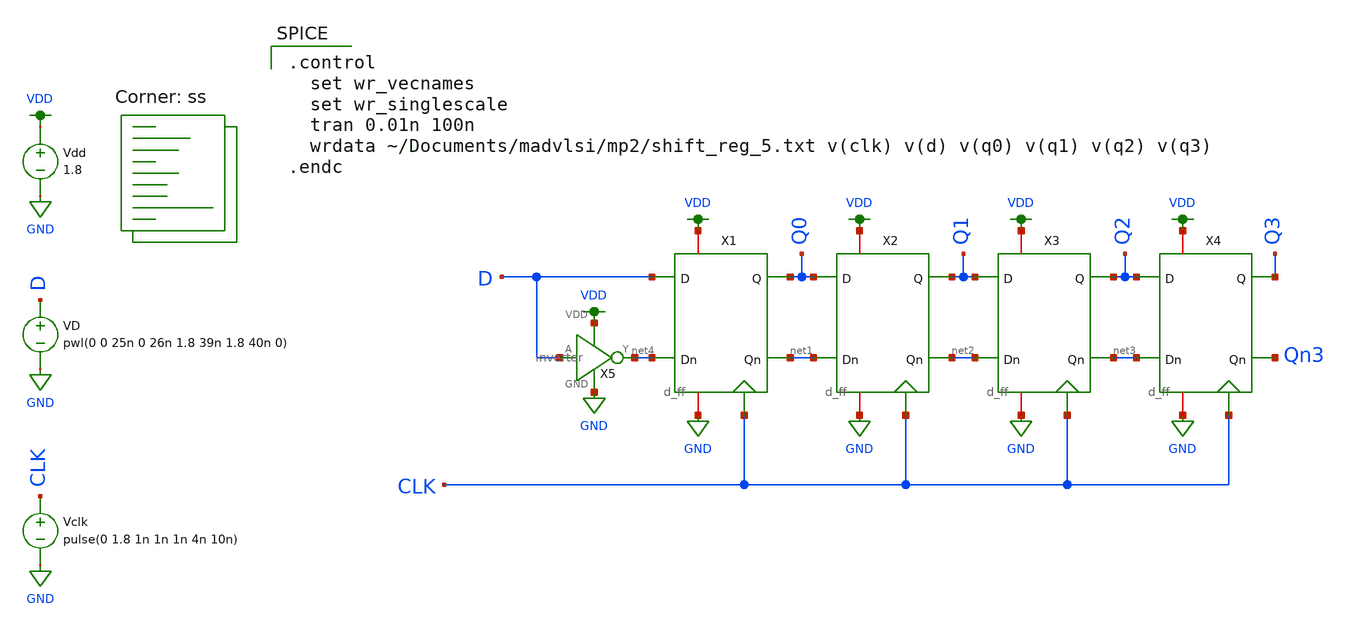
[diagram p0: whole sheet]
** sch_path: mp2/shift_reg_tb.sch
**.subckt shift_reg_tb
X5 VDD D net4 GND inverter
Vdd VDD GND 1.8
VD D GND pwl(0 0 25n 0 26n 1.8 39n 1.8 40n 0)
Vclk CLK GND pulse(0 1.8 1n 1n 1n 4n 10n)
X1 VDD Q0 D net4 net1 GND CLK d_ff
X2 VDD Q1 Q0 net1 net2 GND CLK d_ff
X3 VDD Q2 Q1 net2 net3 GND CLK d_ff
X4 VDD Q3 Q2 net3 Qn3 GND CLK d_ff
**** begin user architecture code
.lib $::SKYWATER_MODELS/sky130.lib.spice ss

.control
  set wr_vecnames
  set wr_singlescale
  tran 0.01n 100n
  wrdata ~/Documents/madvlsi/mp2/shift_reg_5.txt v(clk) v(d) v(q0) v(q1) v(q2) v(q3)
.endc

**** end user architecture code
**.ends

* expanding   symbol:  /home/dt/Documents/madvlsi/mp1/inverter.sym # of pins=4
** sym_path: final/schematics/inverter.sym
** sch_path: final/schematics/inverter.sch
.subckt inverter VDD A Y GND
*.ipin A
*.iopin VDD
*.iopin GND
*.opin Y
XM1 Y A GND GND sky130_fd_pr__nfet_01v8 L={len} W={wid} nf=1 ad='int((nf+1)/2) * W/nf * 0.29' as='int((nf+2)/2) * W/nf * 0.29'
+ pd='2*int((nf+1)/2) * (W/nf + 0.29)' ps='2*int((nf+2)/2) * (W/nf + 0.29)' nrd='0.29 / W' nrs='0.29 / W'
+ sa=0 sb=0 sd=0 mult=1 m=1
XM2 Y A VDD VDD sky130_fd_pr__pfet_01v8 L={len} W={wid} nf=1 ad='int((nf+1)/2) * W/nf * 0.29' as='int((nf+2)/2) * W/nf * 0.29'
+ pd='2*int((nf+1)/2) * (W/nf + 0.29)' ps='2*int((nf+2)/2) * (W/nf + 0.29)' nrd='0.29 / W' nrs='0.29 / W'
+ sa=0 sb=0 sd=0 mult=1 m=1
**** begin user architecture code


.param wid=3 len=0.5


**** end user architecture code
.ends


* expanding   symbol:  d_ff.sym # of pins=7
** sym_path: mp2/d_ff.sym
** sch_path: mp2/d_ff.sch
.subckt d_ff VP Q D Dn Qn VN CLK
*.ipin D
*.ipin Dn
*.ipin CLK
*.iopin VN
*.iopin VP
*.opin Qn
*.opin Q
XM1 net1 CLK Dn VDD sky130_fd_pr__pfet_01v8 L=0.45 W=1 nf=1 ad='int((nf+1)/2) * W/nf * 0.29' as='int((nf+2)/2) * W/nf * 0.29'
+ pd='2*int((nf+1)/2) * (W/nf + 0.29)' ps='2*int((nf+2)/2) * (W/nf + 0.29)' nrd='0.29 / W' nrs='0.29 / W'
+ sa=0 sb=0 sd=0 mult=1 m=1
XM2 VP net4 net1 VDD sky130_fd_pr__pfet_01v8 L=0.15 W=1 nf=1 ad='int((nf+1)/2) * W/nf * 0.29' as='int((nf+2)/2) * W/nf * 0.29'
+ pd='2*int((nf+1)/2) * (W/nf + 0.29)' ps='2*int((nf+2)/2) * (W/nf + 0.29)' nrd='0.29 / W' nrs='0.29 / W'
+ sa=0 sb=0 sd=0 mult=1 m=1
XM3 net2 CLK VP VDD sky130_fd_pr__pfet_01v8 L=0.15 W=1 nf=1 ad='int((nf+1)/2) * W/nf * 0.29' as='int((nf+2)/2) * W/nf * 0.29'
+ pd='2*int((nf+1)/2) * (W/nf + 0.29)' ps='2*int((nf+2)/2) * (W/nf + 0.29)' nrd='0.29 / W' nrs='0.29 / W'
+ sa=0 sb=0 sd=0 mult=1 m=1
XM4 Qn Q net2 VDD sky130_fd_pr__pfet_01v8 L=0.15 W=1 nf=1 ad='int((nf+1)/2) * W/nf * 0.29' as='int((nf+2)/2) * W/nf * 0.29'
+ pd='2*int((nf+1)/2) * (W/nf + 0.29)' ps='2*int((nf+2)/2) * (W/nf + 0.29)' nrd='0.29 / W' nrs='0.29 / W'
+ sa=0 sb=0 sd=0 mult=1 m=1
XM5 net4 CLK D VDD sky130_fd_pr__pfet_01v8 L=0.45 W=1 nf=1 ad='int((nf+1)/2) * W/nf * 0.29' as='int((nf+2)/2) * W/nf * 0.29'
+ pd='2*int((nf+1)/2) * (W/nf + 0.29)' ps='2*int((nf+2)/2) * (W/nf + 0.29)' nrd='0.29 / W' nrs='0.29 / W'
+ sa=0 sb=0 sd=0 mult=1 m=1
XM6 VP net1 net4 VDD sky130_fd_pr__pfet_01v8 L=0.15 W=1 nf=1 ad='int((nf+1)/2) * W/nf * 0.29' as='int((nf+2)/2) * W/nf * 0.29'
+ pd='2*int((nf+1)/2) * (W/nf + 0.29)' ps='2*int((nf+2)/2) * (W/nf + 0.29)' nrd='0.29 / W' nrs='0.29 / W'
+ sa=0 sb=0 sd=0 mult=1 m=1
XM7 net3 CLK VP VDD sky130_fd_pr__pfet_01v8 L=0.15 W=1 nf=1 ad='int((nf+1)/2) * W/nf * 0.29' as='int((nf+2)/2) * W/nf * 0.29'
+ pd='2*int((nf+1)/2) * (W/nf + 0.29)' ps='2*int((nf+2)/2) * (W/nf + 0.29)' nrd='0.29 / W' nrs='0.29 / W'
+ sa=0 sb=0 sd=0 mult=1 m=1
XM8 Q Qn net3 VDD sky130_fd_pr__pfet_01v8 L=0.15 W=1 nf=1 ad='int((nf+1)/2) * W/nf * 0.29' as='int((nf+2)/2) * W/nf * 0.29'
+ pd='2*int((nf+1)/2) * (W/nf + 0.29)' ps='2*int((nf+2)/2) * (W/nf + 0.29)' nrd='0.29 / W' nrs='0.29 / W'
+ sa=0 sb=0 sd=0 mult=1 m=1
XM9 VN CLK net5 GND sky130_fd_pr__nfet_01v8 L=0.15 W=1 nf=1 ad='int((nf+1)/2) * W/nf * 0.29' as='int((nf+2)/2) * W/nf * 0.29'
+ pd='2*int((nf+1)/2) * (W/nf + 0.29)' ps='2*int((nf+2)/2) * (W/nf + 0.29)' nrd='0.29 / W' nrs='0.29 / W'
+ sa=0 sb=0 sd=0 mult=1 m=1
XM10 net4 net1 net5 GND sky130_fd_pr__nfet_01v8 L=0.15 W=1 nf=1 ad='int((nf+1)/2) * W/nf * 0.29' as='int((nf+2)/2) * W/nf * 0.29'
+ pd='2*int((nf+1)/2) * (W/nf + 0.29)' ps='2*int((nf+2)/2) * (W/nf + 0.29)' nrd='0.29 / W' nrs='0.29 / W'
+ sa=0 sb=0 sd=0 mult=1 m=1
XM11 net4 CLK Q GND sky130_fd_pr__nfet_01v8 L=0.45 W=1 nf=1 ad='int((nf+1)/2) * W/nf * 0.29' as='int((nf+2)/2) * W/nf * 0.29'
+ pd='2*int((nf+1)/2) * (W/nf + 0.29)' ps='2*int((nf+2)/2) * (W/nf + 0.29)' nrd='0.29 / W' nrs='0.29 / W'
+ sa=0 sb=0 sd=0 mult=1 m=1
XM12 VN Qn Q GND sky130_fd_pr__nfet_01v8 L=0.15 W=1 nf=1 ad='int((nf+1)/2) * W/nf * 0.29' as='int((nf+2)/2) * W/nf * 0.29'
+ pd='2*int((nf+1)/2) * (W/nf + 0.29)' ps='2*int((nf+2)/2) * (W/nf + 0.29)' nrd='0.29 / W' nrs='0.29 / W'
+ sa=0 sb=0 sd=0 mult=1 m=1
XM13 VN CLK net6 GND sky130_fd_pr__nfet_01v8 L=0.15 W=1 nf=1 ad='int((nf+1)/2) * W/nf * 0.29' as='int((nf+2)/2) * W/nf * 0.29'
+ pd='2*int((nf+1)/2) * (W/nf + 0.29)' ps='2*int((nf+2)/2) * (W/nf + 0.29)' nrd='0.29 / W' nrs='0.29 / W'
+ sa=0 sb=0 sd=0 mult=1 m=1
XM14 net1 net4 net6 GND sky130_fd_pr__nfet_01v8 L=0.15 W=1 nf=1 ad='int((nf+1)/2) * W/nf * 0.29' as='int((nf+2)/2) * W/nf * 0.29'
+ pd='2*int((nf+1)/2) * (W/nf + 0.29)' ps='2*int((nf+2)/2) * (W/nf + 0.29)' nrd='0.29 / W' nrs='0.29 / W'
+ sa=0 sb=0 sd=0 mult=1 m=1
XM15 net1 CLK Qn GND sky130_fd_pr__nfet_01v8 L=0.45 W=1 nf=1 ad='int((nf+1)/2) * W/nf * 0.29' as='int((nf+2)/2) * W/nf * 0.29'
+ pd='2*int((nf+1)/2) * (W/nf + 0.29)' ps='2*int((nf+2)/2) * (W/nf + 0.29)' nrd='0.29 / W' nrs='0.29 / W'
+ sa=0 sb=0 sd=0 mult=1 m=1
XM16 VN Q Qn GND sky130_fd_pr__nfet_01v8 L=0.15 W=1 nf=1 ad='int((nf+1)/2) * W/nf * 0.29' as='int((nf+2)/2) * W/nf * 0.29'
+ pd='2*int((nf+1)/2) * (W/nf + 0.29)' ps='2*int((nf+2)/2) * (W/nf + 0.29)' nrd='0.29 / W' nrs='0.29 / W'
+ sa=0 sb=0 sd=0 mult=1 m=1
.ends

.GLOBAL VDD
.GLOBAL GND
.end
